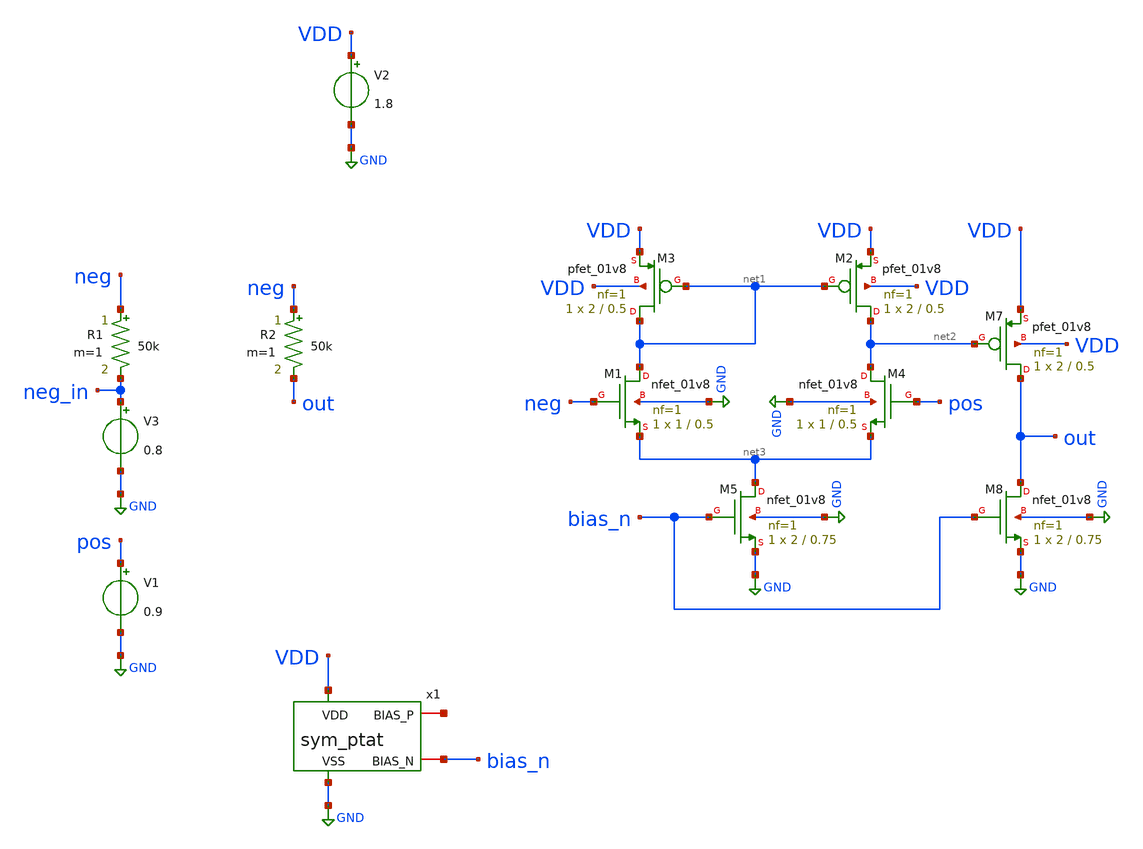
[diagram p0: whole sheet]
** sch_path: schem/op_amp.sch
**.subckt op_amp
XM1 net1 neg net3 GND sky130_fd_pr__nfet_01v8 L=0.5 W=1 nf=1 ad='int((1 + 1)/2) * 1 / 1 * 0.29' as='int((1 + 2)/2) * 1 / 1 * 0.29'
+ pd='2*int((1 + 1)/2) * (1 / 1 + 0.29)' ps='2*int((1 + 2)/2) * (1 / 1 + 0.29)' nrd='0.29 / 1 ' nrs='0.29 / 1 '
+ sa=0 sb=0 sd=0 mult=1 m=1
XM2 net2 net1 VDD VDD sky130_fd_pr__pfet_01v8 L=0.5 W=2 nf=1 ad='int((1 + 1)/2) * 2 / 1 * 0.29' as='int((1 + 2)/2) * 2 / 1 * 0.29'
+ pd='2*int((1 + 1)/2) * (2 / 1 + 0.29)' ps='2*int((1 + 2)/2) * (2 / 1 + 0.29)' nrd='0.29 / 2 ' nrs='0.29 / 2 '
+ sa=0 sb=0 sd=0 mult=1 m=1
XM3 net1 net1 VDD VDD sky130_fd_pr__pfet_01v8 L=0.5 W=2 nf=1 ad='int((1 + 1)/2) * 2 / 1 * 0.29' as='int((1 + 2)/2) * 2 / 1 * 0.29'
+ pd='2*int((1 + 1)/2) * (2 / 1 + 0.29)' ps='2*int((1 + 2)/2) * (2 / 1 + 0.29)' nrd='0.29 / 2 ' nrs='0.29 / 2 '
+ sa=0 sb=0 sd=0 mult=1 m=1
XM4 net2 pos net3 GND sky130_fd_pr__nfet_01v8 L=0.5 W=1 nf=1 ad='int((1 + 1)/2) * 1 / 1 * 0.29' as='int((1 + 2)/2) * 1 / 1 * 0.29'
+ pd='2*int((1 + 1)/2) * (1 / 1 + 0.29)' ps='2*int((1 + 2)/2) * (1 / 1 + 0.29)' nrd='0.29 / 1 ' nrs='0.29 / 1 '
+ sa=0 sb=0 sd=0 mult=1 m=1
XM5 net3 bias_n GND GND sky130_fd_pr__nfet_01v8 L=0.75 W=2 nf=1 ad='int((1 + 1)/2) * 2 / 1 * 0.29' as='int((1 + 2)/2) * 2 / 1 * 0.29'
+ pd='2*int((1 + 1)/2) * (2 / 1 + 0.29)' ps='2*int((1 + 2)/2) * (2 / 1 + 0.29)' nrd='0.29 / 2 ' nrs='0.29 / 2 '
+ sa=0 sb=0 sd=0 mult=1 m=1
V2 VDD GND 1.8
V3 neg_in GND 0.8
XM7 out net2 VDD VDD sky130_fd_pr__pfet_01v8 L=0.5 W=2 nf=1 ad='int((1 + 1)/2) * 2 / 1 * 0.29' as='int((1 + 2)/2) * 2 / 1 * 0.29'
+ pd='2*int((1 + 1)/2) * (2 / 1 + 0.29)' ps='2*int((1 + 2)/2) * (2 / 1 + 0.29)' nrd='0.29 / 2 ' nrs='0.29 / 2 '
+ sa=0 sb=0 sd=0 mult=1 m=1
XM8 out bias_n GND GND sky130_fd_pr__nfet_01v8 L=0.75 W=2 nf=1 ad='int((1 + 1)/2) * 2 / 1 * 0.29' as='int((1 + 2)/2) * 2 / 1 * 0.29'
+ pd='2*int((1 + 1)/2) * (2 / 1 + 0.29)' ps='2*int((1 + 2)/2) * (2 / 1 + 0.29)' nrd='0.29 / 2 ' nrs='0.29 / 2 '
+ sa=0 sb=0 sd=0 mult=1 m=1
V1 pos GND 0.9
R2 neg out 50k m=1
R1 neg neg_in 50k m=1
x1 VDD GND net4 bias_n sym_ptat
**** begin user architecture code


.lib /usr/local/share/pdk/sky130A/libs.tech/ngspice/sky130.lib.spice tt

.tran 1u 5m
.save all
.op

.control
    run
    plot out pos neg_in 1.8 0
.endc

.end


**** end user architecture code
**.ends

* expanding   symbol:  /home/zhixuan/projects/fyp_vco/schem/symbol_repo/sym_ptat.sym # of pins=4
** sym_path: schem/symbol_repo/sym_ptat.sym
** sch_path: schem/symbol_repo/sym_ptat.sch
.subckt sym_ptat VDD VSS BIAS_P BIAS_N
*.ipin VDD
*.ipin VSS
*.iopin BIAS_P
*.iopin BIAS_N
XMN_ptat2 net6 net1 net2 VSS sky130_fd_pr__nfet_01v8 L=0.5 W=2 nf=2 ad='int((2 + 1)/2) * 2 / 2 * 0.29'
+ as='int((2 + 2)/2) * 2 / 2 * 0.29' pd='2*int((2 + 1)/2) * (2 / 2 + 0.29)' ps='2*int((2 + 2)/2) * (2 / 2 + 0.29)'
+ nrd='0.29 / 2 ' nrs='0.29 / 2 ' sa=0 sb=0 sd=0 mult=1 m=1
XMP_diode1 net3 BIAS_P VDD VDD sky130_fd_pr__pfet_01v8 L=0.5 W=2 nf=2 ad='int((2 + 1)/2) * 2 / 2 * 0.29'
+ as='int((2 + 2)/2) * 2 / 2 * 0.29' pd='2*int((2 + 1)/2) * (2 / 2 + 0.29)' ps='2*int((2 + 2)/2) * (2 / 2 + 0.29)'
+ nrd='0.29 / 2 ' nrs='0.29 / 2 ' sa=0 sb=0 sd=0 mult=1 m=1
XMP_mir1_l net4 BIAS_P VDD VDD sky130_fd_pr__pfet_01v8 L=0.5 W=2 nf=2 ad='int((2 + 1)/2) * 2 / 2 * 0.29'
+ as='int((2 + 2)/2) * 2 / 2 * 0.29' pd='2*int((2 + 1)/2) * (2 / 2 + 0.29)' ps='2*int((2 + 2)/2) * (2 / 2 + 0.29)'
+ nrd='0.29 / 2 ' nrs='0.29 / 2 ' sa=0 sb=0 sd=0 mult=1 m=1
XMN_diode2 net5 net1 VSS VSS sky130_fd_pr__nfet_01v8 L=0.5 W=2 nf=4 ad='int((4 + 1)/2) * 2 / 4 * 0.29'
+ as='int((4 + 2)/2) * 2 / 4 * 0.29' pd='2*int((4 + 1)/2) * (2 / 4 + 0.29)' ps='2*int((4 + 2)/2) * (2 / 4 + 0.29)'
+ nrd='0.29 / 2 ' nrs='0.29 / 2 ' sa=0 sb=0 sd=0 mult=1 m=1
XMP_inv BIAS_N BIAS_P VDD VDD sky130_fd_pr__pfet_01v8 L=0.75 W=2 nf=5 ad='int((5 + 1)/2) * 2 / 5 * 0.29'
+ as='int((5 + 2)/2) * 2 / 5 * 0.29' pd='2*int((5 + 1)/2) * (2 / 5 + 0.29)' ps='2*int((5 + 2)/2) * (2 / 5 + 0.29)'
+ nrd='0.29 / 2 ' nrs='0.29 / 2 ' sa=0 sb=0 sd=0 mult=1 m=1
XMP_diode2 BIAS_P BIAS_P net3 VDD sky130_fd_pr__pfet_01v8 L=0.5 W=2 nf=2 ad='int((2 + 1)/2) * 2 / 2 * 0.29'
+ as='int((2 + 2)/2) * 2 / 2 * 0.29' pd='2*int((2 + 1)/2) * (2 / 2 + 0.29)' ps='2*int((2 + 2)/2) * (2 / 2 + 0.29)'
+ nrd='0.29 / 2 ' nrs='0.29 / 2 ' sa=0 sb=0 sd=0 mult=1 m=1
XMP_mir2_l net1 BIAS_P net4 VDD sky130_fd_pr__pfet_01v8 L=0.5 W=2 nf=2 ad='int((2 + 1)/2) * 2 / 2 * 0.29'
+ as='int((2 + 2)/2) * 2 / 2 * 0.29' pd='2*int((2 + 1)/2) * (2 / 2 + 0.29)' ps='2*int((2 + 2)/2) * (2 / 2 + 0.29)'
+ nrd='0.29 / 2 ' nrs='0.29 / 2 ' sa=0 sb=0 sd=0 mult=1 m=1
XMN_ptat1 BIAS_P net1 net6 VSS sky130_fd_pr__nfet_01v8 L=0.5 W=2 nf=2 ad='int((2 + 1)/2) * 2 / 2 * 0.29'
+ as='int((2 + 2)/2) * 2 / 2 * 0.29' pd='2*int((2 + 1)/2) * (2 / 2 + 0.29)' ps='2*int((2 + 2)/2) * (2 / 2 + 0.29)'
+ nrd='0.29 / 2 ' nrs='0.29 / 2 ' sa=0 sb=0 sd=0 mult=1 m=1
XMN_diode1 net1 net1 net5 VSS sky130_fd_pr__nfet_01v8 L=0.5 W=2 nf=4 ad='int((4 + 1)/2) * 2 / 4 * 0.29'
+ as='int((4 + 2)/2) * 2 / 4 * 0.29' pd='2*int((4 + 1)/2) * (2 / 4 + 0.29)' ps='2*int((4 + 2)/2) * (2 / 4 + 0.29)'
+ nrd='0.29 / 2 ' nrs='0.29 / 2 ' sa=0 sb=0 sd=0 mult=1 m=1
XMN_inv BIAS_N BIAS_N VSS VSS sky130_fd_pr__nfet_01v8 L=0.75 W=2.5 nf=2 ad='int((2 + 1)/2) * 2.5 / 2 * 0.29'
+ as='int((2 + 2)/2) * 2.5 / 2 * 0.29' pd='2*int((2 + 1)/2) * (2.5 / 2 + 0.29)' ps='2*int((2 + 2)/2) * (2.5 / 2 + 0.29)'
+ nrd='0.29 / 2.5 ' nrs='0.29 / 2.5 ' sa=0 sb=0 sd=0 mult=1 m=1
XR1 VSS net2 VSS sky130_fd_pr__res_xhigh_po_0p35 L=2.8 mult=1 m=1
XMP_startup net1 VSS VDD VDD sky130_fd_pr__pfet_01v8 L=13 W=1 nf=1 ad='int((1 + 1)/2) * 1 / 1 * 0.29'
+ as='int((1 + 2)/2) * 1 / 1 * 0.29' pd='2*int((1 + 1)/2) * (1 / 1 + 0.29)' ps='2*int((1 + 2)/2) * (1 / 1 + 0.29)'
+ nrd='0.29 / 1 ' nrs='0.29 / 1 ' sa=0 sb=0 sd=0 mult=1 m=1
XMN_diode3 net7 net1 VSS VSS sky130_fd_pr__nfet_01v8 L=0.5 W=2 nf=4 ad='int((4 + 1)/2) * 2 / 4 * 0.29'
+ as='int((4 + 2)/2) * 2 / 4 * 0.29' pd='2*int((4 + 1)/2) * (2 / 4 + 0.29)' ps='2*int((4 + 2)/2) * (2 / 4 + 0.29)'
+ nrd='0.29 / 2 ' nrs='0.29 / 2 ' sa=0 sb=0 sd=0 mult=1 m=1
XMN_diode4 net1 net1 net7 VSS sky130_fd_pr__nfet_01v8 L=0.5 W=2 nf=4 ad='int((4 + 1)/2) * 2 / 4 * 0.29'
+ as='int((4 + 2)/2) * 2 / 4 * 0.29' pd='2*int((4 + 1)/2) * (2 / 4 + 0.29)' ps='2*int((4 + 2)/2) * (2 / 4 + 0.29)'
+ nrd='0.29 / 2 ' nrs='0.29 / 2 ' sa=0 sb=0 sd=0 mult=1 m=1
.ends

.GLOBAL GND
.end
